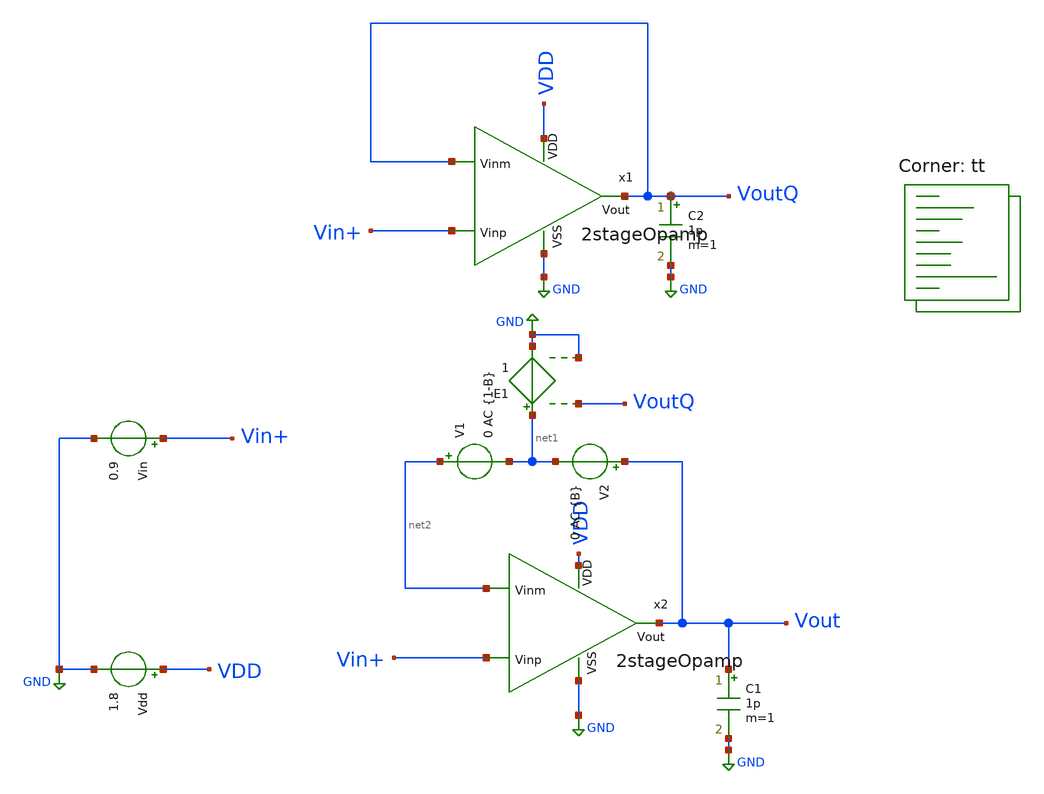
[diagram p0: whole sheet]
** sch_path: xschem/test/xschem/dec24_2stage_tbs/OpenLoopTB_cp.sch
**.subckt OpenLoopTB_cp
Vdd VDD GND 1.8
.save i(vdd)
Vin Vin+ GND 0.9
C1 Vout GND 1p m=1
V2 Vout net1 0 AC {B}
.save i(v2)
V1 net2 net1 0 AC {1-B}
.save i(v1)
C2 VoutQ GND 1p m=1
E1 net1 GND VoutQ GND 1
x1 VDD VoutQ Vin+ VoutQ GND 2stageOpamp
x2 VDD net2 Vin+ Vout GND 2stageOpamp
**** begin user architecture code
.lib $::SKYWATER_MODELS/sky130.lib.spice tt


.param B=0
.savecurrents
.control

save @m.x1.xm5.msky130_fd_pr__pfet_01v8_lvt[gm]
save @m.x1.xm5.msky130_fd_pr__pfet_01v8_lvt[gds]
save @m.x1.xm5.msky130_fd_pr__pfet_01v8_lvt[id]
save @m.x1.xm5.msky130_fd_pr__pfet_01v8_lvt[vgs] -  @m.x1.xm5.msky130_fd_pr__pfet_01v8_lvt[vth]
save @m.x1.xm5.msky130_fd_pr__pfet_01v8_lvt[vds]



save @m.x1.xm1.msky130_fd_pr__nfet_01v8[gm]
save @m.x1.xm1.msky130_fd_pr__nfet_01v8[gds]
save @m.x1.xm1.msky130_fd_pr__nfet_01v8[id]
save @m.x1.xm1.msky130_fd_pr__nfet_01v8[vgs]
save @m.x1.xm1.msky130_fd_pr__nfet_01v8[vds]

save @m.x1.xm3.msky130_fd_pr__nfet_01v8[gm]
save @m.x1.xm3.msky130_fd_pr__nfet_01v8[gds]
save @m.x1.xm3.msky130_fd_pr__nfet_01v8[id]
save @m.x1.xm3.msky130_fd_pr__nfet_01v8[vgs]
save @m.x1.xm3.msky130_fd_pr__nfet_01v8[vds]



save @m.x1.xm7.msky130_fd_pr__pfet_01v8_lvt[gm]
save @m.x1.xm7.msky130_fd_pr__pfet_01v8_lvt[gds]
save @m.x1.xm7.msky130_fd_pr__pfet_01v8_lvt[id]
save @m.x1.xm7.msky130_fd_pr__pfet_01v8_lvt[vgs]
save @m.x1.xm7.msky130_fd_pr__pfet_01v8_lvt[vds]









save @m.x1.xm9.msky130_fd_pr__pfet_01v8_lvt[gm]
save @m.x1.xm9.msky130_fd_pr__pfet_01v8_lvt[gds]
save @m.x1.xm9.msky130_fd_pr__pfet_01v8_lvt[id]
save @m.x1.xm9.msky130_fd_pr__pfet_01v8_lvt[vgs]
save @m.x1.xm9.msky130_fd_pr__pfet_01v8_lvt[vds]

save @m.x1.xm11.msky130_fd_pr__pfet_01v8_lvt[gm]
save @m.x1.xm11.msky130_fd_pr__pfet_01v8_lvt[gds]
save @m.x1.xm11.msky130_fd_pr__pfet_01v8_lvt[id]
save @m.x1.xm11.msky130_fd_pr__pfet_01v8_lvt[vgs]
save @m.x1.xm11.msky130_fd_pr__pfet_01v8_lvt[vds]




save v(Vout)

 op
 ac dec 20 1 1e12
 alterparam B=1
 reset
 ac dec 20 1 1e12
 meas ac freq_at_gain db(v(Vout))=0
 meas ac phase_at_gc ph(v(Vout)) at freq_at_gain

 setplot new
 set curplottitle=Loopgain
 let frequency = ac1.frequency

 let T = (ac1.i(V2)+ac2.i(V1))/(ac1.i(V1)+ac2.i(V2))
 let Tmag = db(T)
 let Tphase = 180 * cph(T)/pi
 let Pm = 180 + Tphase
 plot Tmag Tphase Pm xlog
 plot Tmag xlog

 plot Tphase xlog

 print @m.x1.xm5.msky130_fd_pr__pfet_01v8_lvt[gm]
 print @m.x1.xm5.msky130_fd_pr__pfet_01v8_lvt[gds]
 print @m.x1.xm5.msky130_fd_pr__pfet_01v8_lvt[id]
 print @m.x1.xm5.msky130_fd_pr__pfet_01v8_lvt[vgs]
 print @m.x1.xm5.msky130_fd_pr__pfet_01v8_lvt[vds]

print @m.x1.xm5.msky130_fd_pr__pfet_01v8_lvt[vgs] -  @m.x1.xm5.msky130_fd_pr__pfet_01v8_lvt[vth]

print @m.x1.xm1.msky130_fd_pr__pfet_01v8_lvt[vgs] -  @m.x1.xm1.msky130_fd_pr__pfet_01v8_lvt[vth]

 print @m.x1.xm7.msky130_fd_pr__pfet_01v8_lvt[gm]
 print @m.x1.xm7.msky130_fd_pr__pfet_01v8_lvt[gds]
 print @m.x1.xm7.msky130_fd_pr__pfet_01v8_lvt[id]
 print @m.x1.xm7.msky130_fd_pr__pfet_01v8_lvt[vgs]
 print @m.x1.xm7.msky130_fd_pr__pfet_01v8_lvt[vds]

 print @m.x1.xm9.msky130_fd_pr__pfet_01v8_lvt[gm]
 print @m.x1.xm9.msky130_fd_pr__pfet_01v8_lvt[gds]
 print @m.x1.xm9.msky130_fd_pr__pfet_01v8_lvt[id]
 print @m.x1.xm9.msky130_fd_pr__pfet_01v8_lvt[vgs]
 print @m.x1.xm9.msky130_fd_pr__pfet_01v8_lvt[vds]

 print @m.x1.xm11.msky130_fd_pr__pfet_01v8_lvt[gm]
 print @m.x1.xm11.msky130_fd_pr__pfet_01v8_lvt[gds]
 print @m.x1.xm11.msky130_fd_pr__pfet_01v8_lvt[id]
 print @m.x1.xm11.msky130_fd_pr__pfet_01v8_lvt[vgs]
 print @m.x1.xm11.msky130_fd_pr__pfet_01v8_lvt[vds]

 print @m.x1.xm10.msky130_fd_pr__pfet_01v8_lvt[gm]
 print @m.x1.xm10.msky130_fd_pr__pfet_01v8_lvt[gds]
 print @m.x1.xm10.msky130_fd_pr__pfet_01v8_lvt[id]
 print @m.x1.xm10.msky130_fd_pr__pfet_01v8_lvt[vgs]
 print @m.x1.xm10.msky130_fd_pr__pfet_01v8_lvt[vds]



 print @m.x1.xm1.msky130_fd_pr__nfet_01v8[gm]
 print @m.x1.xm1.msky130_fd_pr__nfet_01v8[gds]
 print @m.x1.xm1.msky130_fd_pr__nfet_01v8[id]
 print @m.x1.xm1.msky130_fd_pr__nfet_01v8[vgs] - @m.x1.xm1.msky130_fd_pr__nfet_01v8[vth]
 print @m.x1.xm1.msky130_fd_pr__nfet_01v8[vds]

 print @m.x1.xm3.msky130_fd_pr__nfet_01v8[gm]
 print @m.x1.xm3.msky130_fd_pr__nfet_01v8[gds]
 print @m.x1.xm3.msky130_fd_pr__nfet_01v8[id]
 print @m.x1.xm3.msky130_fd_pr__nfet_01v8[vgs]
 print @m.x1.xm3.msky130_fd_pr__nfet_01v8[vds]




 write OpenLoopTB.raw


.endc


**** end user architecture code
**.ends

* expanding   symbol:  amplifiers/dec24/2stageOpamp.sym # of pins=5
** sym_path: amplifiers/dec24/2stageOpamp.sym
** sch_path: amplifiers/dec24/2stageOpamp.sch
.subckt 2stageOpamp VDD Vinm Vinp Vout VSS
*.ipin Vinm
*.ipin Vinp
*.opin Vout
*.ipin VSS
*.ipin VDD
XM8 Vout net1 VSS VSS sky130_fd_pr__nfet_01v8 L=1 W=6 nf=1 ad='int((nf+1)/2) * W/nf * 0.29' as='int((nf+2)/2) * W/nf * 0.29'
+ pd='2*int((nf+1)/2) * (W/nf + 0.29)' ps='2*int((nf+2)/2) * (W/nf + 0.29)' nrd='0.29 / W' nrs='0.29 / W'
+ sa=0 sb=0 sd=0 mult=8 m=8
XM2 Vout Vb1 VDD VDD sky130_fd_pr__pfet_01v8_lvt L=1 W=9 nf=1 ad='int((nf+1)/2) * W/nf * 0.29' as='int((nf+2)/2) * W/nf * 0.29'
+ pd='2*int((nf+1)/2) * (W/nf + 0.29)' ps='2*int((nf+2)/2) * (W/nf + 0.29)' nrd='0.29 / W' nrs='0.29 / W'
+ sa=0 sb=0 sd=0 mult=3 m=3
XM5 net5 Vb3 net6 VSS sky130_fd_pr__nfet_01v8 L=1 W=4 nf=1 ad='int((nf+1)/2) * W/nf * 0.29' as='int((nf+2)/2) * W/nf * 0.29'
+ pd='2*int((nf+1)/2) * (W/nf + 0.29)' ps='2*int((nf+2)/2) * (W/nf + 0.29)' nrd='0.29 / W' nrs='0.29 / W'
+ sa=0 sb=0 sd=0 mult=3 m=3
XM17 net1 Vb3 net7 VSS sky130_fd_pr__nfet_01v8 L=1 W=4 nf=1 ad='int((nf+1)/2) * W/nf * 0.29' as='int((nf+2)/2) * W/nf * 0.29'
+ pd='2*int((nf+1)/2) * (W/nf + 0.29)' ps='2*int((nf+2)/2) * (W/nf + 0.29)' nrd='0.29 / W' nrs='0.29 / W'
+ sa=0 sb=0 sd=0 mult=3 m=3
XM3 net6 net5 VSS VSS sky130_fd_pr__nfet_01v8 L=1 W=8 nf=1 ad='int((nf+1)/2) * W/nf * 0.29' as='int((nf+2)/2) * W/nf * 0.29'
+ pd='2*int((nf+1)/2) * (W/nf + 0.29)' ps='2*int((nf+2)/2) * (W/nf + 0.29)' nrd='0.29 / W' nrs='0.29 / W'
+ sa=0 sb=0 sd=0 mult=1 m=1
XM19 net7 net5 VSS VSS sky130_fd_pr__nfet_01v8 L=1 W=8 nf=1 ad='int((nf+1)/2) * W/nf * 0.29' as='int((nf+2)/2) * W/nf * 0.29'
+ pd='2*int((nf+1)/2) * (W/nf + 0.29)' ps='2*int((nf+2)/2) * (W/nf + 0.29)' nrd='0.29 / W' nrs='0.29 / W'
+ sa=0 sb=0 sd=0 mult=1 m=1
V1 Vb1 GND 1.1
V2 Vb2 GND 0.7
V3 Vb3 GND 0.9
XM11 net8 Vb1 VDD VDD sky130_fd_pr__pfet_01v8_lvt L=1 W=9 nf=1 ad='int((nf+1)/2) * W/nf * 0.29' as='int((nf+2)/2) * W/nf * 0.29'
+ pd='2*int((nf+1)/2) * (W/nf + 0.29)' ps='2*int((nf+2)/2) * (W/nf + 0.29)' nrd='0.29 / W' nrs='0.29 / W'
+ sa=0 sb=0 sd=0 mult=2 m=2
XM1 net6 Vinm net8 VDD sky130_fd_pr__pfet_01v8_lvt L=1 W=8 nf=1 ad='int((nf+1)/2) * W/nf * 0.29' as='int((nf+2)/2) * W/nf * 0.29'
+ pd='2*int((nf+1)/2) * (W/nf + 0.29)' ps='2*int((nf+2)/2) * (W/nf + 0.29)' nrd='0.29 / W' nrs='0.29 / W'
+ sa=0 sb=0 sd=0 mult=3 m=3
XM15 net7 Vinp net8 VDD sky130_fd_pr__pfet_01v8_lvt L=1 W=8 nf=1 ad='int((nf+1)/2) * W/nf * 0.29' as='int((nf+2)/2) * W/nf * 0.29'
+ pd='2*int((nf+1)/2) * (W/nf + 0.29)' ps='2*int((nf+2)/2) * (W/nf + 0.29)' nrd='0.29 / W' nrs='0.29 / W'
+ sa=0 sb=0 sd=0 mult=3 m=3
XM7 net3 Vb1 VDD VDD sky130_fd_pr__pfet_01v8_lvt L=1 W=9 nf=1 ad='int((nf+1)/2) * W/nf * 0.29' as='int((nf+2)/2) * W/nf * 0.29'
+ pd='2*int((nf+1)/2) * (W/nf + 0.29)' ps='2*int((nf+2)/2) * (W/nf + 0.29)' nrd='0.29 / W' nrs='0.29 / W'
+ sa=0 sb=0 sd=0 mult=1 m=1
XM21 net4 Vb1 VDD VDD sky130_fd_pr__pfet_01v8_lvt L=1 W=9 nf=1 ad='int((nf+1)/2) * W/nf * 0.29' as='int((nf+2)/2) * W/nf * 0.29'
+ pd='2*int((nf+1)/2) * (W/nf + 0.29)' ps='2*int((nf+2)/2) * (W/nf + 0.29)' nrd='0.29 / W' nrs='0.29 / W'
+ sa=0 sb=0 sd=0 mult=1 m=1
XM9 net5 Vb2 net3 VDD sky130_fd_pr__pfet_01v8_lvt L=1 W=9 nf=1 ad='int((nf+1)/2) * W/nf * 0.29' as='int((nf+2)/2) * W/nf * 0.29'
+ pd='2*int((nf+1)/2) * (W/nf + 0.29)' ps='2*int((nf+2)/2) * (W/nf + 0.29)' nrd='0.29 / W' nrs='0.29 / W'
+ sa=0 sb=0 sd=0 mult=1 m=1
XM23 net1 Vb2 net4 VDD sky130_fd_pr__pfet_01v8_lvt L=1 W=9 nf=1 ad='int((nf+1)/2) * W/nf * 0.29' as='int((nf+2)/2) * W/nf * 0.29'
+ pd='2*int((nf+1)/2) * (W/nf + 0.29)' ps='2*int((nf+2)/2) * (W/nf + 0.29)' nrd='0.29 / W' nrs='0.29 / W'
+ sa=0 sb=0 sd=0 mult=1 m=1
XC4 net2 Vout sky130_fd_pr__cap_mim_m3_2 W=7 L=7 MF=4 m=4
R4 net1 net2 7k m=1
.ends

.GLOBAL GND
.end
